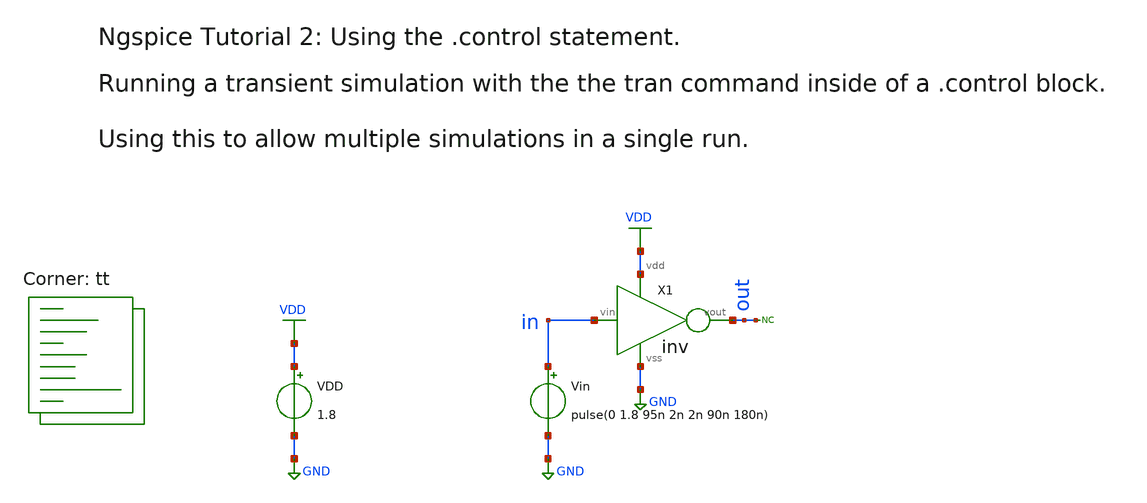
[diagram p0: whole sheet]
** sch_path: xsch/tut/ngspice_tut2.sch
**.subckt ngspice_tut2
Vin in GND pulse(0 1.8 95n 2n 2n 90n 180n)
VDD VDD GND 1.8
X1 in out VDD GND inv
* noconn out
**** begin user architecture code



* control language script

.control

tran 100p 500n						; simulation command 1
set xbrushwidth=2						; set linewidth of the graph
gnuplot ngspice_tut2_tran_plot.plt in out						; plot the simulation results
write $inputdir/outtran.out v(in) v(out)
reset

dc vin 0 1.8 0.01						; simulation command 2
gnuplot ngspice_tut2_dc_plot.plot in	out					; v(in) not required because it is the x-axis already
write $inputdir/outdc.out v(out)
.endc

.end



.lib $::SKYWATER_MODELS/sky130.lib.spice tt
**** end user architecture code
**.ends
.GLOBAL VDD
.GLOBAL GND
.end
